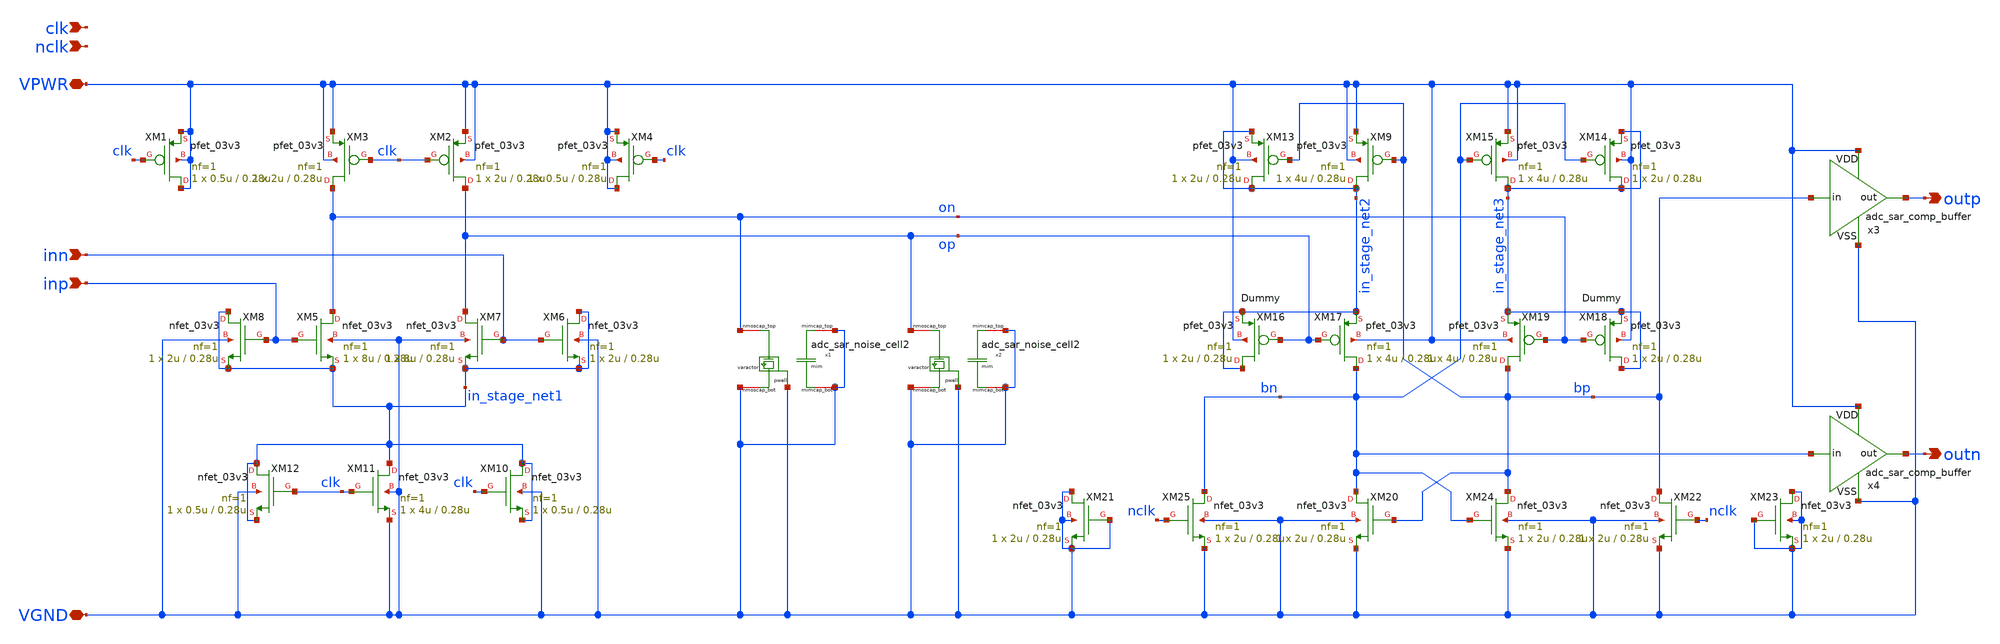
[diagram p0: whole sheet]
** sch_path: adc_sar_comp_circuit.sch
**.subckt adc_sar_comp_circuit VPWR VGND clk nclk inp inn outp outn
*.iopin VPWR
*.iopin VGND
*.ipin clk
*.ipin nclk
*.ipin inp
*.ipin inn
*.opin outp
*.opin outn
XM1 VPWR clk VPWR VPWR pfet_03v3 L=0.28u W=0.5u nf=1 ad='int((nf+1)/2) * W/nf * 0.18u' as='int((nf+2)/2) * W/nf * 0.18u'
+ pd='2*int((nf+1)/2) * (W/nf + 0.18u)' ps='2*int((nf+2)/2) * (W/nf + 0.18u)' nrd='0.18u / W' nrs='0.18u / W'
+ sa=0 sb=0 sd=0 m=1
XM2 op clk VPWR VPWR pfet_03v3 L=0.28u W=2u nf=1 ad='int((nf+1)/2) * W/nf * 0.18u' as='int((nf+2)/2) * W/nf * 0.18u'
+ pd='2*int((nf+1)/2) * (W/nf + 0.18u)' ps='2*int((nf+2)/2) * (W/nf + 0.18u)' nrd='0.18u / W' nrs='0.18u / W'
+ sa=0 sb=0 sd=0 m=1
XM3 on clk VPWR VPWR pfet_03v3 L=0.28u W=2u nf=1 ad='int((nf+1)/2) * W/nf * 0.18u' as='int((nf+2)/2) * W/nf * 0.18u'
+ pd='2*int((nf+1)/2) * (W/nf + 0.18u)' ps='2*int((nf+2)/2) * (W/nf + 0.18u)' nrd='0.18u / W' nrs='0.18u / W'
+ sa=0 sb=0 sd=0 m=1
XM4 VPWR clk VPWR VPWR pfet_03v3 L=0.28u W=0.5u nf=1 ad='int((nf+1)/2) * W/nf * 0.18u' as='int((nf+2)/2) * W/nf * 0.18u'
+ pd='2*int((nf+1)/2) * (W/nf + 0.18u)' ps='2*int((nf+2)/2) * (W/nf + 0.18u)' nrd='0.18u / W' nrs='0.18u / W'
+ sa=0 sb=0 sd=0 m=1
x1 VGND VGND on VGND VGND adc_sar_noise_cell2
x2 VGND VGND op VGND VGND adc_sar_noise_cell2
XM5 on inp in_stage_net1 VGND nfet_03v3 L=0.28u W=8u nf=1 ad='int((nf+1)/2) * W/nf * 0.18u' as='int((nf+2)/2) * W/nf * 0.18u'
+ pd='2*int((nf+1)/2) * (W/nf + 0.18u)' ps='2*int((nf+2)/2) * (W/nf + 0.18u)' nrd='0.18u / W' nrs='0.18u / W'
+ sa=0 sb=0 sd=0 m=1
XM6 in_stage_net1 inn in_stage_net1 VGND nfet_03v3 L=0.28u W=2u nf=1 ad='int((nf+1)/2) * W/nf * 0.18u'
+ as='int((nf+2)/2) * W/nf * 0.18u' pd='2*int((nf+1)/2) * (W/nf + 0.18u)' ps='2*int((nf+2)/2) * (W/nf + 0.18u)'
+ nrd='0.18u / W' nrs='0.18u / W' sa=0 sb=0 sd=0 m=1
XM7 op inn in_stage_net1 VGND nfet_03v3 L=0.28u W=8u nf=1 ad='int((nf+1)/2) * W/nf * 0.18u' as='int((nf+2)/2) * W/nf * 0.18u'
+ pd='2*int((nf+1)/2) * (W/nf + 0.18u)' ps='2*int((nf+2)/2) * (W/nf + 0.18u)' nrd='0.18u / W' nrs='0.18u / W'
+ sa=0 sb=0 sd=0 m=1
XM8 in_stage_net1 inp in_stage_net1 VGND nfet_03v3 L=0.28u W=2u nf=1 ad='int((nf+1)/2) * W/nf * 0.18u'
+ as='int((nf+2)/2) * W/nf * 0.18u' pd='2*int((nf+1)/2) * (W/nf + 0.18u)' ps='2*int((nf+2)/2) * (W/nf + 0.18u)'
+ nrd='0.18u / W' nrs='0.18u / W' sa=0 sb=0 sd=0 m=1
XM10 in_stage_net1 clk in_stage_net1 VGND nfet_03v3 L=0.28u W=0.5u nf=1 ad='int((nf+1)/2) * W/nf * 0.18u'
+ as='int((nf+2)/2) * W/nf * 0.18u' pd='2*int((nf+1)/2) * (W/nf + 0.18u)' ps='2*int((nf+2)/2) * (W/nf + 0.18u)'
+ nrd='0.18u / W' nrs='0.18u / W' sa=0 sb=0 sd=0 m=1
XM11 in_stage_net1 clk VGND VGND nfet_03v3 L=0.28u W=4u nf=1 ad='int((nf+1)/2) * W/nf * 0.18u' as='int((nf+2)/2) * W/nf * 0.18u'
+ pd='2*int((nf+1)/2) * (W/nf + 0.18u)' ps='2*int((nf+2)/2) * (W/nf + 0.18u)' nrd='0.18u / W' nrs='0.18u / W'
+ sa=0 sb=0 sd=0 m=1
XM12 in_stage_net1 clk in_stage_net1 VGND nfet_03v3 L=0.28u W=0.5u nf=1 ad='int((nf+1)/2) * W/nf * 0.18u'
+ as='int((nf+2)/2) * W/nf * 0.18u' pd='2*int((nf+1)/2) * (W/nf + 0.18u)' ps='2*int((nf+2)/2) * (W/nf + 0.18u)'
+ nrd='0.18u / W' nrs='0.18u / W' sa=0 sb=0 sd=0 m=1
XM9 in_stage_net2 bp VPWR VPWR pfet_03v3 L=0.28u W=4u nf=1 ad='int((nf+1)/2) * W/nf * 0.18u' as='int((nf+2)/2) * W/nf * 0.18u'
+ pd='2*int((nf+1)/2) * (W/nf + 0.18u)' ps='2*int((nf+2)/2) * (W/nf + 0.18u)' nrd='0.18u / W' nrs='0.18u / W'
+ sa=0 sb=0 sd=0 m=1
XM13 in_stage_net2 bp in_stage_net2 VPWR pfet_03v3 L=0.28u W=2u nf=1 ad='int((nf+1)/2) * W/nf * 0.18u'
+ as='int((nf+2)/2) * W/nf * 0.18u' pd='2*int((nf+1)/2) * (W/nf + 0.18u)' ps='2*int((nf+2)/2) * (W/nf + 0.18u)'
+ nrd='0.18u / W' nrs='0.18u / W' sa=0 sb=0 sd=0 m=1
XM14 in_stage_net3 bn in_stage_net3 VPWR pfet_03v3 L=0.28u W=2u nf=1 ad='int((nf+1)/2) * W/nf * 0.18u'
+ as='int((nf+2)/2) * W/nf * 0.18u' pd='2*int((nf+1)/2) * (W/nf + 0.18u)' ps='2*int((nf+2)/2) * (W/nf + 0.18u)'
+ nrd='0.18u / W' nrs='0.18u / W' sa=0 sb=0 sd=0 m=1
XM15 in_stage_net3 bn VPWR VPWR pfet_03v3 L=0.28u W=4u nf=1 ad='int((nf+1)/2) * W/nf * 0.18u' as='int((nf+2)/2) * W/nf * 0.18u'
+ pd='2*int((nf+1)/2) * (W/nf + 0.18u)' ps='2*int((nf+2)/2) * (W/nf + 0.18u)' nrd='0.18u / W' nrs='0.18u / W'
+ sa=0 sb=0 sd=0 m=1
XM16 in_stage_net2 op in_stage_net2 VPWR pfet_03v3 L=0.28u W=2u nf=1 ad='int((nf+1)/2) * W/nf * 0.18u'
+ as='int((nf+2)/2) * W/nf * 0.18u' pd='2*int((nf+1)/2) * (W/nf + 0.18u)' ps='2*int((nf+2)/2) * (W/nf + 0.18u)'
+ nrd='0.18u / W' nrs='0.18u / W' sa=0 sb=0 sd=0 m=1
XM17 bn op in_stage_net2 VPWR pfet_03v3 L=0.28u W=4u nf=1 ad='int((nf+1)/2) * W/nf * 0.18u' as='int((nf+2)/2) * W/nf * 0.18u'
+ pd='2*int((nf+1)/2) * (W/nf + 0.18u)' ps='2*int((nf+2)/2) * (W/nf + 0.18u)' nrd='0.18u / W' nrs='0.18u / W'
+ sa=0 sb=0 sd=0 m=1
XM18 in_stage_net3 on in_stage_net3 VPWR pfet_03v3 L=0.28u W=2u nf=1 ad='int((nf+1)/2) * W/nf * 0.18u'
+ as='int((nf+2)/2) * W/nf * 0.18u' pd='2*int((nf+1)/2) * (W/nf + 0.18u)' ps='2*int((nf+2)/2) * (W/nf + 0.18u)'
+ nrd='0.18u / W' nrs='0.18u / W' sa=0 sb=0 sd=0 m=1
XM19 bp on in_stage_net3 VPWR pfet_03v3 L=0.28u W=4u nf=1 ad='int((nf+1)/2) * W/nf * 0.18u' as='int((nf+2)/2) * W/nf * 0.18u'
+ pd='2*int((nf+1)/2) * (W/nf + 0.18u)' ps='2*int((nf+2)/2) * (W/nf + 0.18u)' nrd='0.18u / W' nrs='0.18u / W'
+ sa=0 sb=0 sd=0 m=1
XM21 VGND VGND VGND VGND nfet_03v3 L=0.28u W=2u nf=1 ad='int((nf+1)/2) * W/nf * 0.18u' as='int((nf+2)/2) * W/nf * 0.18u'
+ pd='2*int((nf+1)/2) * (W/nf + 0.18u)' ps='2*int((nf+2)/2) * (W/nf + 0.18u)' nrd='0.18u / W' nrs='0.18u / W'
+ sa=0 sb=0 sd=0 m=1
XM20 bn bp VGND VGND nfet_03v3 L=0.28u W=2u nf=1 ad='int((nf+1)/2) * W/nf * 0.18u' as='int((nf+2)/2) * W/nf * 0.18u'
+ pd='2*int((nf+1)/2) * (W/nf + 0.18u)' ps='2*int((nf+2)/2) * (W/nf + 0.18u)' nrd='0.18u / W' nrs='0.18u / W'
+ sa=0 sb=0 sd=0 m=1
XM22 bp nclk VGND VGND nfet_03v3 L=0.28u W=2u nf=1 ad='int((nf+1)/2) * W/nf * 0.18u' as='int((nf+2)/2) * W/nf * 0.18u'
+ pd='2*int((nf+1)/2) * (W/nf + 0.18u)' ps='2*int((nf+2)/2) * (W/nf + 0.18u)' nrd='0.18u / W' nrs='0.18u / W'
+ sa=0 sb=0 sd=0 m=1
XM23 VGND VGND VGND VGND nfet_03v3 L=0.28u W=2u nf=1 ad='int((nf+1)/2) * W/nf * 0.18u' as='int((nf+2)/2) * W/nf * 0.18u'
+ pd='2*int((nf+1)/2) * (W/nf + 0.18u)' ps='2*int((nf+2)/2) * (W/nf + 0.18u)' nrd='0.18u / W' nrs='0.18u / W'
+ sa=0 sb=0 sd=0 m=1
XM24 bp bn VGND VGND nfet_03v3 L=0.28u W=2u nf=1 ad='int((nf+1)/2) * W/nf * 0.18u' as='int((nf+2)/2) * W/nf * 0.18u'
+ pd='2*int((nf+1)/2) * (W/nf + 0.18u)' ps='2*int((nf+2)/2) * (W/nf + 0.18u)' nrd='0.18u / W' nrs='0.18u / W'
+ sa=0 sb=0 sd=0 m=1
XM25 bn nclk VGND VGND nfet_03v3 L=0.28u W=2u nf=1 ad='int((nf+1)/2) * W/nf * 0.18u' as='int((nf+2)/2) * W/nf * 0.18u'
+ pd='2*int((nf+1)/2) * (W/nf + 0.18u)' ps='2*int((nf+2)/2) * (W/nf + 0.18u)' nrd='0.18u / W' nrs='0.18u / W'
+ sa=0 sb=0 sd=0 m=1
x3 VPWR VGND bp outp adc_sar_comp_buffer
x4 VPWR VGND bn outn adc_sar_comp_buffer
**.ends
.end
